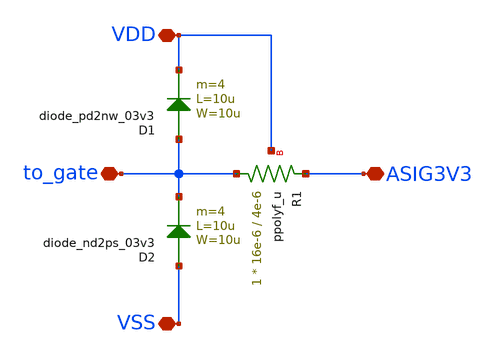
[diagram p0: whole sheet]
** sch_path: resources/Integration/Chipathon2025_pads/xschem/symbols/io_secondary_3p3/io_secondary_3p3.sch
**.subckt io_secondary_3p3 VSS VDD to_gate ASIG3V3
*.iopin VSS
*.iopin VDD
*.iopin to_gate
*.iopin ASIG3V3
XR1 to_gate ASIG3V3 VDD ppolyf_u r_width=16e-6 r_length=4e-6 m=1
D2 VSS to_gate diode_nd2ps_03v3 area='10u * 10u ' pj='2*10u + 2*10u ' m=4
D1 to_gate VDD diode_pd2nw_03v3 area='10u * 10u ' pj='2*10u + 2*10u ' m=4
**.ends
.end
